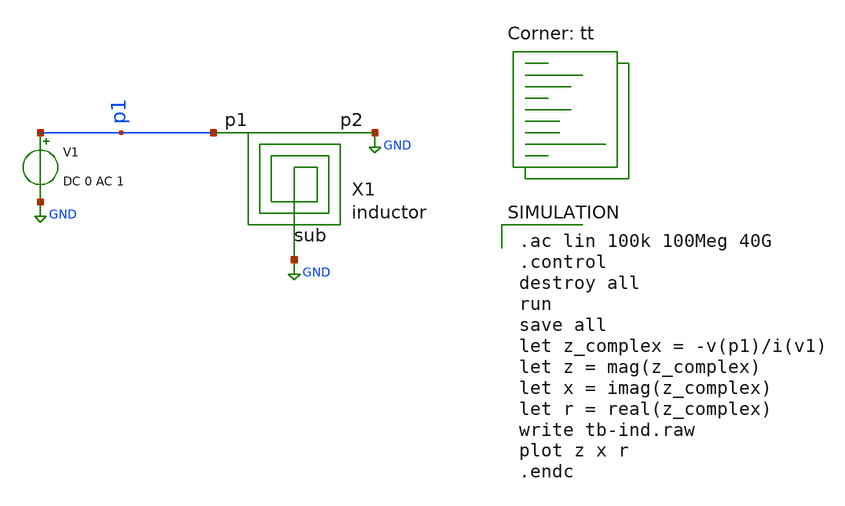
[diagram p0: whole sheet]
** sch_path: MICRO/tb-1.sch
**.subckt tb-1
X1 p1 GND GND inductor
V1 p1 GND DC 0 AC 1
**** begin user architecture code
.lib $::SKYWATER_MODELS/sky130.lib.spice tt

.ac lin 100k 100Meg 40G
.control
destroy all
run
save all
let z_complex = -v(p1)/i(v1)
let z = mag(z_complex)
let x = imag(z_complex)
let r = real(z_complex)
write tb-ind.raw
plot z x r
.endc

**** end user architecture code
**.ends

* expanding   symbol:  MICRO/inductor.sym # of pins=3
** sym_path: MICRO/inductor.sym
** sch_path: MICRO/inductor.sch
.subckt inductor p1 p2 sub
*.iopin p1
*.iopin p2
*.iopin sub
L p1 net2 1.006n m=1
R net2 p2 2.857 m=1
Cs1 p1 net3 33.97f m=1
Cs2 net1 p2 36.78f m=1
Rs1 sub net3 27.37 m=1
Rs2 net1 sub -9 m=1
.ends

.GLOBAL GND
.end
